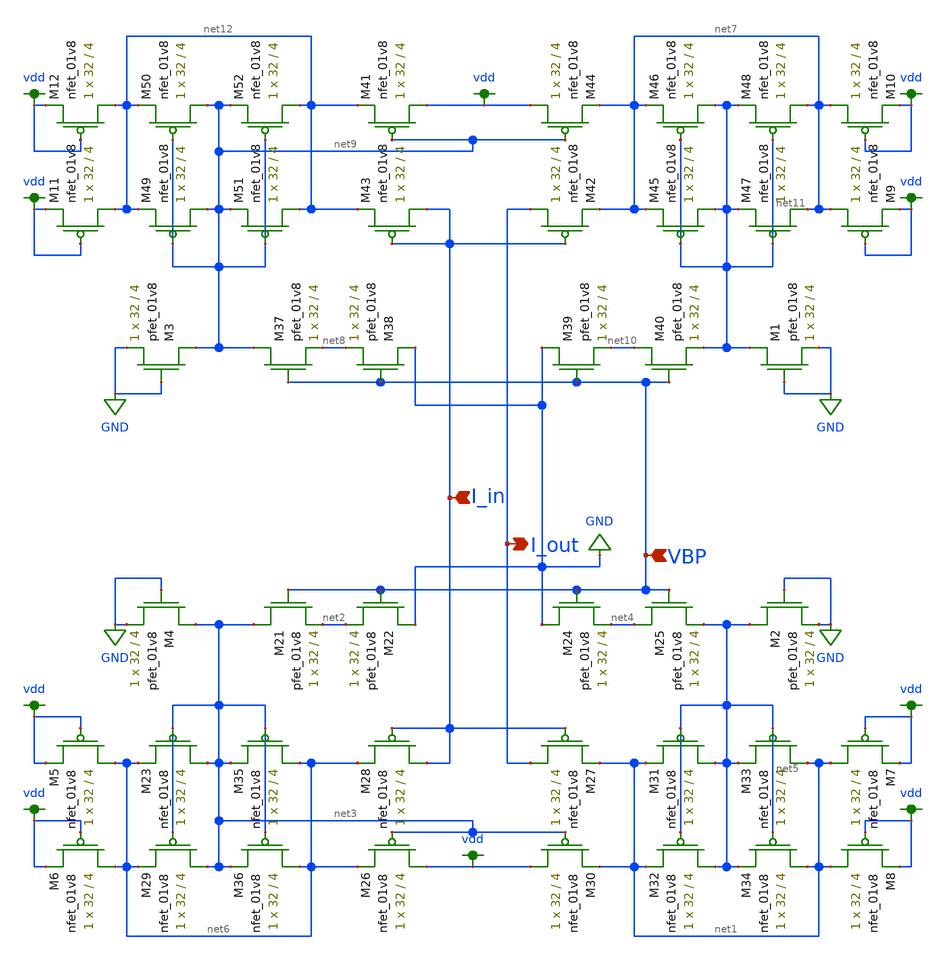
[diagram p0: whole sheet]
** sch_path: schemas/LDS_first_current_mirror.sch
**.subckt LDS_first_current_mirror I_out VBP I_in
*.opin I_out
*.ipin VBP
*.ipin I_in
XM21 net3 VBP net2 VDD sky130_fd_pr__pfet_01v8 L=4 W=32 nf=1 ad='int((nf+1)/2) * W/nf * 0.29' as='int((nf+2)/2) * W/nf * 0.29'
+ pd='2*int((nf+1)/2) * (W/nf + 0.29)' ps='2*int((nf+2)/2) * (W/nf + 0.29)' nrd='0.29 / W' nrs='0.29 / W'
+ sa=0 sb=0 sd=0 mult=1 m=1
XM22 GND VBP net2 VDD sky130_fd_pr__pfet_01v8 L=4 W=32 nf=1 ad='int((nf+1)/2) * W/nf * 0.29' as='int((nf+2)/2) * W/nf * 0.29'
+ pd='2*int((nf+1)/2) * (W/nf + 0.29)' ps='2*int((nf+2)/2) * (W/nf + 0.29)' nrd='0.29 / W' nrs='0.29 / W'
+ sa=0 sb=0 sd=0 mult=1 m=1
XM24 GND VBP net4 VDD sky130_fd_pr__pfet_01v8 L=4 W=32 nf=1 ad='int((nf+1)/2) * W/nf * 0.29' as='int((nf+2)/2) * W/nf * 0.29'
+ pd='2*int((nf+1)/2) * (W/nf + 0.29)' ps='2*int((nf+2)/2) * (W/nf + 0.29)' nrd='0.29 / W' nrs='0.29 / W'
+ sa=0 sb=0 sd=0 mult=1 m=1
XM25 net4 VBP net5 VDD sky130_fd_pr__pfet_01v8 L=4 W=32 nf=1 ad='int((nf+1)/2) * W/nf * 0.29' as='int((nf+2)/2) * W/nf * 0.29'
+ pd='2*int((nf+1)/2) * (W/nf + 0.29)' ps='2*int((nf+2)/2) * (W/nf + 0.29)' nrd='0.29 / W' nrs='0.29 / W'
+ sa=0 sb=0 sd=0 mult=1 m=1
XM26 vdd net3 net6 GND sky130_fd_pr__nfet_01v8 L=4 W=32 nf=1 ad='int((nf+1)/2) * W/nf * 0.29' as='int((nf+2)/2) * W/nf * 0.29'
+ pd='2*int((nf+1)/2) * (W/nf + 0.29)' ps='2*int((nf+2)/2) * (W/nf + 0.29)' nrd='0.29 / W' nrs='0.29 / W'
+ sa=0 sb=0 sd=0 mult=1 m=1
XM27 I_out I_in net1 GND sky130_fd_pr__nfet_01v8 L=4 W=32 nf=1 ad='int((nf+1)/2) * W/nf * 0.29' as='int((nf+2)/2) * W/nf * 0.29'
+ pd='2*int((nf+1)/2) * (W/nf + 0.29)' ps='2*int((nf+2)/2) * (W/nf + 0.29)' nrd='0.29 / W' nrs='0.29 / W'
+ sa=0 sb=0 sd=0 mult=1 m=1
XM28 I_in I_in net6 GND sky130_fd_pr__nfet_01v8 L=4 W=32 nf=1 ad='int((nf+1)/2) * W/nf * 0.29' as='int((nf+2)/2) * W/nf * 0.29'
+ pd='2*int((nf+1)/2) * (W/nf + 0.29)' ps='2*int((nf+2)/2) * (W/nf + 0.29)' nrd='0.29 / W' nrs='0.29 / W'
+ sa=0 sb=0 sd=0 mult=1 m=1
XM30 vdd net3 net1 GND sky130_fd_pr__nfet_01v8 L=4 W=32 nf=1 ad='int((nf+1)/2) * W/nf * 0.29' as='int((nf+2)/2) * W/nf * 0.29'
+ pd='2*int((nf+1)/2) * (W/nf + 0.29)' ps='2*int((nf+2)/2) * (W/nf + 0.29)' nrd='0.29 / W' nrs='0.29 / W'
+ sa=0 sb=0 sd=0 mult=1 m=1
XM31 net5 net5 net1 GND sky130_fd_pr__nfet_01v8 L=4 W=32 nf=1 ad='int((nf+1)/2) * W/nf * 0.29' as='int((nf+2)/2) * W/nf * 0.29'
+ pd='2*int((nf+1)/2) * (W/nf + 0.29)' ps='2*int((nf+2)/2) * (W/nf + 0.29)' nrd='0.29 / W' nrs='0.29 / W'
+ sa=0 sb=0 sd=0 mult=1 m=1
XM32 net5 net5 net1 GND sky130_fd_pr__nfet_01v8 L=4 W=32 nf=1 ad='int((nf+1)/2) * W/nf * 0.29' as='int((nf+2)/2) * W/nf * 0.29'
+ pd='2*int((nf+1)/2) * (W/nf + 0.29)' ps='2*int((nf+2)/2) * (W/nf + 0.29)' nrd='0.29 / W' nrs='0.29 / W'
+ sa=0 sb=0 sd=0 mult=1 m=1
XM33 net1 net5 net5 GND sky130_fd_pr__nfet_01v8 L=4 W=32 nf=1 ad='int((nf+1)/2) * W/nf * 0.29' as='int((nf+2)/2) * W/nf * 0.29'
+ pd='2*int((nf+1)/2) * (W/nf + 0.29)' ps='2*int((nf+2)/2) * (W/nf + 0.29)' nrd='0.29 / W' nrs='0.29 / W'
+ sa=0 sb=0 sd=0 mult=1 m=1
XM34 net1 net5 net5 GND sky130_fd_pr__nfet_01v8 L=4 W=32 nf=1 ad='int((nf+1)/2) * W/nf * 0.29' as='int((nf+2)/2) * W/nf * 0.29'
+ pd='2*int((nf+1)/2) * (W/nf + 0.29)' ps='2*int((nf+2)/2) * (W/nf + 0.29)' nrd='0.29 / W' nrs='0.29 / W'
+ sa=0 sb=0 sd=0 mult=1 m=1
XM23 net3 net3 net6 GND sky130_fd_pr__nfet_01v8 L=4 W=32 nf=1 ad='int((nf+1)/2) * W/nf * 0.29' as='int((nf+2)/2) * W/nf * 0.29'
+ pd='2*int((nf+1)/2) * (W/nf + 0.29)' ps='2*int((nf+2)/2) * (W/nf + 0.29)' nrd='0.29 / W' nrs='0.29 / W'
+ sa=0 sb=0 sd=0 mult=1 m=1
XM29 net3 net3 net6 GND sky130_fd_pr__nfet_01v8 L=4 W=32 nf=1 ad='int((nf+1)/2) * W/nf * 0.29' as='int((nf+2)/2) * W/nf * 0.29'
+ pd='2*int((nf+1)/2) * (W/nf + 0.29)' ps='2*int((nf+2)/2) * (W/nf + 0.29)' nrd='0.29 / W' nrs='0.29 / W'
+ sa=0 sb=0 sd=0 mult=1 m=1
XM35 net6 net3 net3 GND sky130_fd_pr__nfet_01v8 L=4 W=32 nf=1 ad='int((nf+1)/2) * W/nf * 0.29' as='int((nf+2)/2) * W/nf * 0.29'
+ pd='2*int((nf+1)/2) * (W/nf + 0.29)' ps='2*int((nf+2)/2) * (W/nf + 0.29)' nrd='0.29 / W' nrs='0.29 / W'
+ sa=0 sb=0 sd=0 mult=1 m=1
XM36 net6 net3 net3 GND sky130_fd_pr__nfet_01v8 L=4 W=32 nf=1 ad='int((nf+1)/2) * W/nf * 0.29' as='int((nf+2)/2) * W/nf * 0.29'
+ pd='2*int((nf+1)/2) * (W/nf + 0.29)' ps='2*int((nf+2)/2) * (W/nf + 0.29)' nrd='0.29 / W' nrs='0.29 / W'
+ sa=0 sb=0 sd=0 mult=1 m=1
XM37 net9 VBP net8 VDD sky130_fd_pr__pfet_01v8 L=4 W=32 nf=1 ad='int((nf+1)/2) * W/nf * 0.29' as='int((nf+2)/2) * W/nf * 0.29'
+ pd='2*int((nf+1)/2) * (W/nf + 0.29)' ps='2*int((nf+2)/2) * (W/nf + 0.29)' nrd='0.29 / W' nrs='0.29 / W'
+ sa=0 sb=0 sd=0 mult=1 m=1
XM38 GND VBP net8 VDD sky130_fd_pr__pfet_01v8 L=4 W=32 nf=1 ad='int((nf+1)/2) * W/nf * 0.29' as='int((nf+2)/2) * W/nf * 0.29'
+ pd='2*int((nf+1)/2) * (W/nf + 0.29)' ps='2*int((nf+2)/2) * (W/nf + 0.29)' nrd='0.29 / W' nrs='0.29 / W'
+ sa=0 sb=0 sd=0 mult=1 m=1
XM39 GND VBP net10 VDD sky130_fd_pr__pfet_01v8 L=4 W=32 nf=1 ad='int((nf+1)/2) * W/nf * 0.29' as='int((nf+2)/2) * W/nf * 0.29'
+ pd='2*int((nf+1)/2) * (W/nf + 0.29)' ps='2*int((nf+2)/2) * (W/nf + 0.29)' nrd='0.29 / W' nrs='0.29 / W'
+ sa=0 sb=0 sd=0 mult=1 m=1
XM40 net10 VBP net11 VDD sky130_fd_pr__pfet_01v8 L=4 W=32 nf=1 ad='int((nf+1)/2) * W/nf * 0.29' as='int((nf+2)/2) * W/nf * 0.29'
+ pd='2*int((nf+1)/2) * (W/nf + 0.29)' ps='2*int((nf+2)/2) * (W/nf + 0.29)' nrd='0.29 / W' nrs='0.29 / W'
+ sa=0 sb=0 sd=0 mult=1 m=1
XM41 vdd net9 net12 GND sky130_fd_pr__nfet_01v8 L=4 W=32 nf=1 ad='int((nf+1)/2) * W/nf * 0.29' as='int((nf+2)/2) * W/nf * 0.29'
+ pd='2*int((nf+1)/2) * (W/nf + 0.29)' ps='2*int((nf+2)/2) * (W/nf + 0.29)' nrd='0.29 / W' nrs='0.29 / W'
+ sa=0 sb=0 sd=0 mult=1 m=1
XM42 I_out I_in net7 GND sky130_fd_pr__nfet_01v8 L=4 W=32 nf=1 ad='int((nf+1)/2) * W/nf * 0.29' as='int((nf+2)/2) * W/nf * 0.29'
+ pd='2*int((nf+1)/2) * (W/nf + 0.29)' ps='2*int((nf+2)/2) * (W/nf + 0.29)' nrd='0.29 / W' nrs='0.29 / W'
+ sa=0 sb=0 sd=0 mult=1 m=1
XM43 I_in I_in net12 GND sky130_fd_pr__nfet_01v8 L=4 W=32 nf=1 ad='int((nf+1)/2) * W/nf * 0.29' as='int((nf+2)/2) * W/nf * 0.29'
+ pd='2*int((nf+1)/2) * (W/nf + 0.29)' ps='2*int((nf+2)/2) * (W/nf + 0.29)' nrd='0.29 / W' nrs='0.29 / W'
+ sa=0 sb=0 sd=0 mult=1 m=1
XM44 vdd net9 net7 GND sky130_fd_pr__nfet_01v8 L=4 W=32 nf=1 ad='int((nf+1)/2) * W/nf * 0.29' as='int((nf+2)/2) * W/nf * 0.29'
+ pd='2*int((nf+1)/2) * (W/nf + 0.29)' ps='2*int((nf+2)/2) * (W/nf + 0.29)' nrd='0.29 / W' nrs='0.29 / W'
+ sa=0 sb=0 sd=0 mult=1 m=1
XM45 net11 net11 net7 GND sky130_fd_pr__nfet_01v8 L=4 W=32 nf=1 ad='int((nf+1)/2) * W/nf * 0.29' as='int((nf+2)/2) * W/nf * 0.29'
+ pd='2*int((nf+1)/2) * (W/nf + 0.29)' ps='2*int((nf+2)/2) * (W/nf + 0.29)' nrd='0.29 / W' nrs='0.29 / W'
+ sa=0 sb=0 sd=0 mult=1 m=1
XM46 net11 net11 net7 GND sky130_fd_pr__nfet_01v8 L=4 W=32 nf=1 ad='int((nf+1)/2) * W/nf * 0.29' as='int((nf+2)/2) * W/nf * 0.29'
+ pd='2*int((nf+1)/2) * (W/nf + 0.29)' ps='2*int((nf+2)/2) * (W/nf + 0.29)' nrd='0.29 / W' nrs='0.29 / W'
+ sa=0 sb=0 sd=0 mult=1 m=1
XM47 net7 net11 net11 GND sky130_fd_pr__nfet_01v8 L=4 W=32 nf=1 ad='int((nf+1)/2) * W/nf * 0.29' as='int((nf+2)/2) * W/nf * 0.29'
+ pd='2*int((nf+1)/2) * (W/nf + 0.29)' ps='2*int((nf+2)/2) * (W/nf + 0.29)' nrd='0.29 / W' nrs='0.29 / W'
+ sa=0 sb=0 sd=0 mult=1 m=1
XM48 net7 net11 net11 GND sky130_fd_pr__nfet_01v8 L=4 W=32 nf=1 ad='int((nf+1)/2) * W/nf * 0.29' as='int((nf+2)/2) * W/nf * 0.29'
+ pd='2*int((nf+1)/2) * (W/nf + 0.29)' ps='2*int((nf+2)/2) * (W/nf + 0.29)' nrd='0.29 / W' nrs='0.29 / W'
+ sa=0 sb=0 sd=0 mult=1 m=1
XM49 net9 net9 net12 GND sky130_fd_pr__nfet_01v8 L=4 W=32 nf=1 ad='int((nf+1)/2) * W/nf * 0.29' as='int((nf+2)/2) * W/nf * 0.29'
+ pd='2*int((nf+1)/2) * (W/nf + 0.29)' ps='2*int((nf+2)/2) * (W/nf + 0.29)' nrd='0.29 / W' nrs='0.29 / W'
+ sa=0 sb=0 sd=0 mult=1 m=1
XM50 net9 net9 net12 GND sky130_fd_pr__nfet_01v8 L=4 W=32 nf=1 ad='int((nf+1)/2) * W/nf * 0.29' as='int((nf+2)/2) * W/nf * 0.29'
+ pd='2*int((nf+1)/2) * (W/nf + 0.29)' ps='2*int((nf+2)/2) * (W/nf + 0.29)' nrd='0.29 / W' nrs='0.29 / W'
+ sa=0 sb=0 sd=0 mult=1 m=1
XM51 net12 net9 net9 GND sky130_fd_pr__nfet_01v8 L=4 W=32 nf=1 ad='int((nf+1)/2) * W/nf * 0.29' as='int((nf+2)/2) * W/nf * 0.29'
+ pd='2*int((nf+1)/2) * (W/nf + 0.29)' ps='2*int((nf+2)/2) * (W/nf + 0.29)' nrd='0.29 / W' nrs='0.29 / W'
+ sa=0 sb=0 sd=0 mult=1 m=1
XM52 net12 net9 net9 GND sky130_fd_pr__nfet_01v8 L=4 W=32 nf=1 ad='int((nf+1)/2) * W/nf * 0.29' as='int((nf+2)/2) * W/nf * 0.29'
+ pd='2*int((nf+1)/2) * (W/nf + 0.29)' ps='2*int((nf+2)/2) * (W/nf + 0.29)' nrd='0.29 / W' nrs='0.29 / W'
+ sa=0 sb=0 sd=0 mult=1 m=1
XM1 net11 GND GND VDD sky130_fd_pr__pfet_01v8 L=4 W=32 nf=1 ad='int((nf+1)/2) * W/nf * 0.29' as='int((nf+2)/2) * W/nf * 0.29'
+ pd='2*int((nf+1)/2) * (W/nf + 0.29)' ps='2*int((nf+2)/2) * (W/nf + 0.29)' nrd='0.29 / W' nrs='0.29 / W'
+ sa=0 sb=0 sd=0 mult=1 m=1
XM2 net5 GND GND VDD sky130_fd_pr__pfet_01v8 L=4 W=32 nf=1 ad='int((nf+1)/2) * W/nf * 0.29' as='int((nf+2)/2) * W/nf * 0.29'
+ pd='2*int((nf+1)/2) * (W/nf + 0.29)' ps='2*int((nf+2)/2) * (W/nf + 0.29)' nrd='0.29 / W' nrs='0.29 / W'
+ sa=0 sb=0 sd=0 mult=1 m=1
XM3 net9 GND GND VDD sky130_fd_pr__pfet_01v8 L=4 W=32 nf=1 ad='int((nf+1)/2) * W/nf * 0.29' as='int((nf+2)/2) * W/nf * 0.29'
+ pd='2*int((nf+1)/2) * (W/nf + 0.29)' ps='2*int((nf+2)/2) * (W/nf + 0.29)' nrd='0.29 / W' nrs='0.29 / W'
+ sa=0 sb=0 sd=0 mult=1 m=1
XM4 net3 GND GND VDD sky130_fd_pr__pfet_01v8 L=4 W=32 nf=1 ad='int((nf+1)/2) * W/nf * 0.29' as='int((nf+2)/2) * W/nf * 0.29'
+ pd='2*int((nf+1)/2) * (W/nf + 0.29)' ps='2*int((nf+2)/2) * (W/nf + 0.29)' nrd='0.29 / W' nrs='0.29 / W'
+ sa=0 sb=0 sd=0 mult=1 m=1
XM5 net6 vdd vdd GND sky130_fd_pr__nfet_01v8 L=4 W=32 nf=1 ad='int((nf+1)/2) * W/nf * 0.29' as='int((nf+2)/2) * W/nf * 0.29'
+ pd='2*int((nf+1)/2) * (W/nf + 0.29)' ps='2*int((nf+2)/2) * (W/nf + 0.29)' nrd='0.29 / W' nrs='0.29 / W'
+ sa=0 sb=0 sd=0 mult=1 m=1
XM6 net6 vdd vdd GND sky130_fd_pr__nfet_01v8 L=4 W=32 nf=1 ad='int((nf+1)/2) * W/nf * 0.29' as='int((nf+2)/2) * W/nf * 0.29'
+ pd='2*int((nf+1)/2) * (W/nf + 0.29)' ps='2*int((nf+2)/2) * (W/nf + 0.29)' nrd='0.29 / W' nrs='0.29 / W'
+ sa=0 sb=0 sd=0 mult=1 m=1
XM7 net1 vdd vdd GND sky130_fd_pr__nfet_01v8 L=4 W=32 nf=1 ad='int((nf+1)/2) * W/nf * 0.29' as='int((nf+2)/2) * W/nf * 0.29'
+ pd='2*int((nf+1)/2) * (W/nf + 0.29)' ps='2*int((nf+2)/2) * (W/nf + 0.29)' nrd='0.29 / W' nrs='0.29 / W'
+ sa=0 sb=0 sd=0 mult=1 m=1
XM8 net1 vdd vdd GND sky130_fd_pr__nfet_01v8 L=4 W=32 nf=1 ad='int((nf+1)/2) * W/nf * 0.29' as='int((nf+2)/2) * W/nf * 0.29'
+ pd='2*int((nf+1)/2) * (W/nf + 0.29)' ps='2*int((nf+2)/2) * (W/nf + 0.29)' nrd='0.29 / W' nrs='0.29 / W'
+ sa=0 sb=0 sd=0 mult=1 m=1
XM9 net7 vdd vdd GND sky130_fd_pr__nfet_01v8 L=4 W=32 nf=1 ad='int((nf+1)/2) * W/nf * 0.29' as='int((nf+2)/2) * W/nf * 0.29'
+ pd='2*int((nf+1)/2) * (W/nf + 0.29)' ps='2*int((nf+2)/2) * (W/nf + 0.29)' nrd='0.29 / W' nrs='0.29 / W'
+ sa=0 sb=0 sd=0 mult=1 m=1
XM10 net7 vdd vdd GND sky130_fd_pr__nfet_01v8 L=4 W=32 nf=1 ad='int((nf+1)/2) * W/nf * 0.29' as='int((nf+2)/2) * W/nf * 0.29'
+ pd='2*int((nf+1)/2) * (W/nf + 0.29)' ps='2*int((nf+2)/2) * (W/nf + 0.29)' nrd='0.29 / W' nrs='0.29 / W'
+ sa=0 sb=0 sd=0 mult=1 m=1
XM11 net12 vdd vdd GND sky130_fd_pr__nfet_01v8 L=4 W=32 nf=1 ad='int((nf+1)/2) * W/nf * 0.29' as='int((nf+2)/2) * W/nf * 0.29'
+ pd='2*int((nf+1)/2) * (W/nf + 0.29)' ps='2*int((nf+2)/2) * (W/nf + 0.29)' nrd='0.29 / W' nrs='0.29 / W'
+ sa=0 sb=0 sd=0 mult=1 m=1
XM12 net12 vdd vdd GND sky130_fd_pr__nfet_01v8 L=4 W=32 nf=1 ad='int((nf+1)/2) * W/nf * 0.29' as='int((nf+2)/2) * W/nf * 0.29'
+ pd='2*int((nf+1)/2) * (W/nf + 0.29)' ps='2*int((nf+2)/2) * (W/nf + 0.29)' nrd='0.29 / W' nrs='0.29 / W'
+ sa=0 sb=0 sd=0 mult=1 m=1
**.ends
.GLOBAL vdd
.GLOBAL GND
.end
